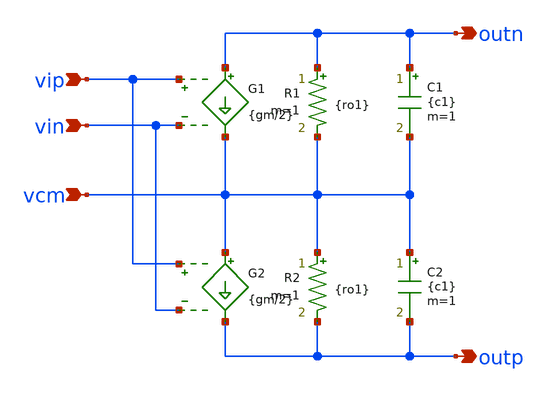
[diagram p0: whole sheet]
** sch_path: modules/ideal_op_diff.sch
**.subckt ideal_op_diff vip vin outp outn vcm
*.ipin vip
*.ipin vin
*.opin outp
*.opin outn
*.ipin vcm
G1 outn vcm vip vin {gm/2}
G2 vcm outp vip vin {gm/2}
R1 outn vcm {ro1} m=1
R2 vcm outp {ro1} m=1
C1 outn vcm {c1} m=1
C2 vcm outp {c1} m=1
**.ends
.end
